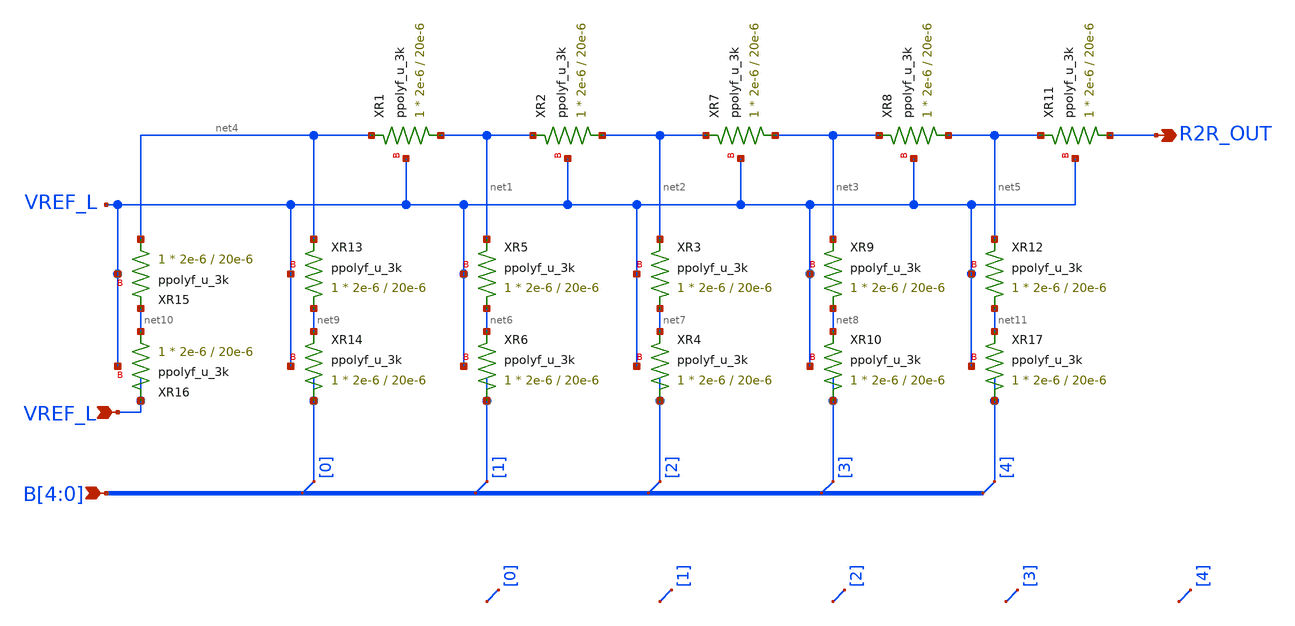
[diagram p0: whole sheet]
** sch_path: xschem/r2r.sch
**.subckt r2r R2R_OUT VREF_L B[4],B[3],B[2],B[1],B[0]
*.opin R2R_OUT
*.ipin VREF_L
*.ipin B[4],B[3],B[2],B[1],B[0]
XR1 net1 net4 VREF_L ppolyf_u_3k r_width=2e-6 r_length=20e-6 m=1
XR2 net2 net1 VREF_L ppolyf_u_3k r_width=2e-6 r_length=20e-6 m=1
XR5 net6 net1 VREF_L ppolyf_u_3k r_width=2e-6 r_length=20e-6 m=1
XR6 B[1] net6 VREF_L ppolyf_u_3k r_width=2e-6 r_length=20e-6 m=1
XR3 net7 net2 VREF_L ppolyf_u_3k r_width=2e-6 r_length=20e-6 m=1
XR4 B[2] net7 VREF_L ppolyf_u_3k r_width=2e-6 r_length=20e-6 m=1
XR7 net3 net2 VREF_L ppolyf_u_3k r_width=2e-6 r_length=20e-6 m=1
XR8 net5 net3 VREF_L ppolyf_u_3k r_width=2e-6 r_length=20e-6 m=1
XR9 net8 net3 VREF_L ppolyf_u_3k r_width=2e-6 r_length=20e-6 m=1
XR10 B[3] net8 VREF_L ppolyf_u_3k r_width=2e-6 r_length=20e-6 m=1
XR13 net9 net4 VREF_L ppolyf_u_3k r_width=2e-6 r_length=20e-6 m=1
XR14 B[0] net9 VREF_L ppolyf_u_3k r_width=2e-6 r_length=20e-6 m=1
XR15 net4 net10 VREF_L ppolyf_u_3k r_width=2e-6 r_length=20e-6 m=1
XR16 net10 VREF_L VREF_L ppolyf_u_3k r_width=2e-6 r_length=20e-6 m=1
XR11 R2R_OUT net5 VREF_L ppolyf_u_3k r_width=2e-6 r_length=20e-6 m=1
XR12 net11 net5 VREF_L ppolyf_u_3k r_width=2e-6 r_length=20e-6 m=1
XR17 B[4] net11 VREF_L ppolyf_u_3k r_width=2e-6 r_length=20e-6 m=1
* tap: B[4:0] --> B[0]
* tap: B[4:0] --> B[1]
* tap: B[4:0] --> B[2]
* tap: B[4:0] --> B[3]
* tap: B[4:0] --> B[4]
* tap: #net13 --> #net12
* tap: #net15 --> #net14
* tap: #net17 --> #net16
* tap: #net19 --> #net18
* tap: #net21 --> #net20
**.ends
.end
